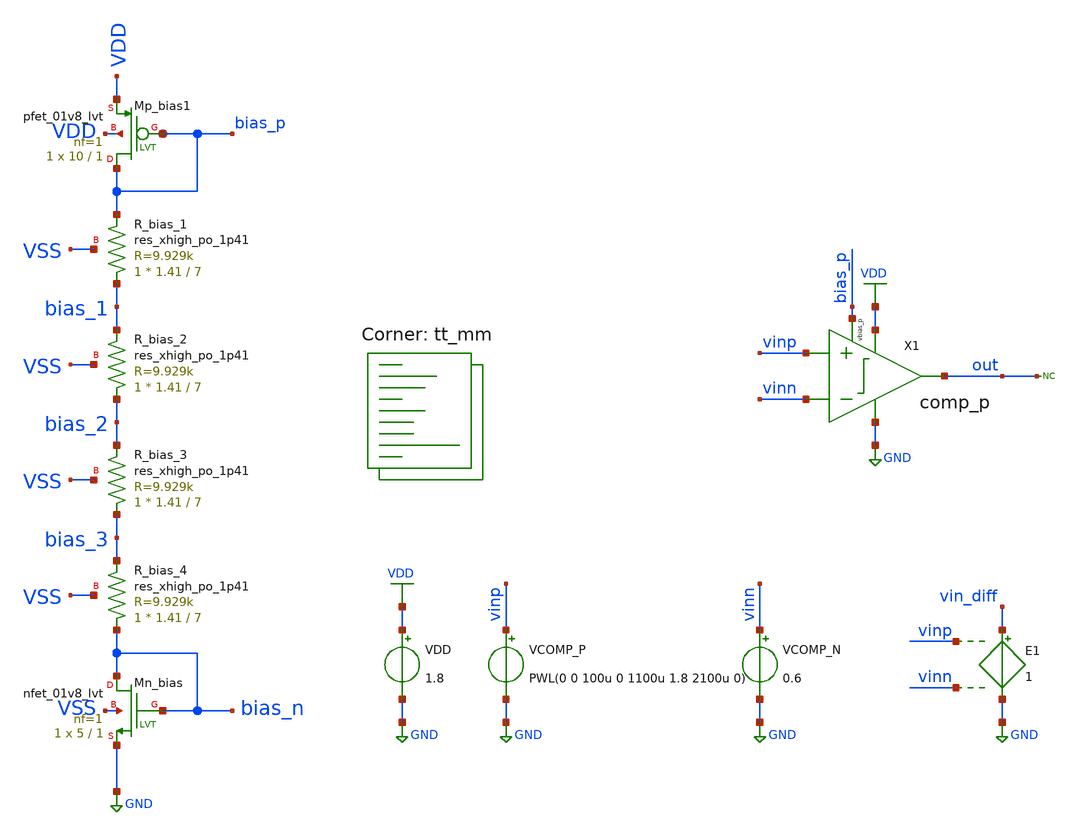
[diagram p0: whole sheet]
** sch_path: xsch/tb/comp_p/tb_comp_p_tran_sweep_mc.sch
**.subckt tb_comp_p_tran_sweep_mc
VDD VDD GND 1.8
* noconn out
VCOMP_N vinn GND 0.6
VCOMP_P vinp GND PWL(0 0 100u 0 1100u 1.8 2100u 0)
E1 vin_diff GND vinp vinn 1
XR_bias_1 bias_1 bias_p VSS sky130_fd_pr__res_xhigh_po_1p41 L=7 mult=1 m=1
XMn_bias bias_n bias_n GND VSS sky130_fd_pr__nfet_01v8_lvt L=1 W=5 nf=1 ad='int((nf+1)/2) * W/nf * 0.29'
+ as='int((nf+2)/2) * W/nf * 0.29' pd='2*int((nf+1)/2) * (W/nf + 0.29)' ps='2*int((nf+2)/2) * (W/nf + 0.29)'
+ nrd='0.29 / W' nrs='0.29 / W' sa=0 sb=0 sd=0 mult=1 m=1
XMp_bias1 bias_p bias_p VDD VDD sky130_fd_pr__pfet_01v8_lvt L=1 W=10 nf=1 ad='int((nf+1)/2) * W/nf * 0.29'
+ as='int((nf+2)/2) * W/nf * 0.29' pd='2*int((nf+1)/2) * (W/nf + 0.29)' ps='2*int((nf+2)/2) * (W/nf + 0.29)'
+ nrd='0.29 / W' nrs='0.29 / W' sa=0 sb=0 sd=0 mult=1 m=1
XR_bias_2 bias_2 bias_1 VSS sky130_fd_pr__res_xhigh_po_1p41 L=7 mult=1 m=1
XR_bias_3 bias_3 bias_2 VSS sky130_fd_pr__res_xhigh_po_1p41 L=7 mult=1 m=1
XR_bias_4 bias_n bias_3 VSS sky130_fd_pr__res_xhigh_po_1p41 L=7 mult=1 m=1
X1 vinp vinn bias_p out VDD GND comp_p
**** begin user architecture code



* control language script
.save X_COMP_P.latch_right
.save X_COMP_P.latch_left
.save vinp vinn out vdd
.save X_COMP_P.tail
.save bias_n

.control
set singlescale
set wr_vecnames
let mc_runs = 200
let run = 0

let v_th = vector(mc_runs)
let v_tl = vector(mc_runs)
let v_hyst = vector(mc_runs)
let v_offset = vector(mc_runs)
let design_point = vector(mc_runs) ; lets me plot quantities vs mc run

while run <= mc_runs
	tran 0.1u 2100u

	meas tran v_cross_lh FIND v(vinp) when v(out)=0.9 RISE=1
	meas tran v_cross_hl FIND v(vinp) when v(out)=0.9 FALL=1

	let v_th[run] = v_cross_lh-0.6
	let v_tl[run] = v_cross_hl-0.6
	let v_hyst[run] = v_th[run] - v_tl[run]
	let v_offset[run] = v_th[run] + v_tl[run]

	echo V_th: $&v_th
	echo V_tl: $&v_tl
	echo V_hyst: $&v_hyst
	echo V_offset: $&v_offset

	reset
	let run = run + 1;
end

plot tran1.v(out) tran2.v(out) tran3.v(out) tran4.v(out) tran5.v(out) tran6.v(out) tran7.v(out)
+ tran8.v(out) tran9.v(out) tran10.v(out) tran1.v(vinp) tran1.v(vinn)

wrdata tb_comp_p_tran_sweep_mc_vth.txt v_th vs design_point
wrdata tb_comp_p_tran_sweep_mc_vhyst.txt v_hyst vs design_point

rusage

.endc
.end



.lib $::SKYWATER_MODELS/sky130.lib.spice tt_mm
**** end user architecture code
**.ends

* expanding   symbol:  /home/bmott/ttsky25b_tiny_chaos/xsch/ip/comparators/comp_p/comp_p.sym # of
*+ pins=6
** sym_path: /home/bmott/ttsky25b_tiny_chaos/xsch/ip/comparators/comp_p/comp_p.sym
** sch_path: /home/bmott/ttsky25b_tiny_chaos/xsch/ip/comparators/comp_p/comp_p.sch
.subckt comp_p vinp vinn vbias_p vout vdd vss
*.iopin vdd
*.iopin vss
*.ipin vbias_p
*.ipin vinn
*.ipin vinp
*.opin vout
XMp_inn1 latch_left vinn tail vdd sky130_fd_pr__pfet_01v8_lvt L=0.35 W=10 nf=1 ad='int((nf+1)/2) * W/nf * 0.29'
+ as='int((nf+2)/2) * W/nf * 0.29' pd='2*int((nf+1)/2) * (W/nf + 0.29)' ps='2*int((nf+2)/2) * (W/nf + 0.29)'
+ nrd='0.29 / W' nrs='0.29 / W' sa=0 sb=0 sd=0 mult=4 m=4
XMp_inp1 latch_right vinp tail vdd sky130_fd_pr__pfet_01v8_lvt L=0.35 W=10 nf=1 ad='int((nf+1)/2) * W/nf * 0.29'
+ as='int((nf+2)/2) * W/nf * 0.29' pd='2*int((nf+1)/2) * (W/nf + 0.29)' ps='2*int((nf+2)/2) * (W/nf + 0.29)'
+ nrd='0.29 / W' nrs='0.29 / W' sa=0 sb=0 sd=0 mult=4 m=4
XMn_diode_left1 latch_left latch_left vss vss sky130_fd_pr__nfet_01v8_lvt L=1 W=4 nf=1 ad='int((nf+1)/2) * W/nf * 0.29'
+ as='int((nf+2)/2) * W/nf * 0.29' pd='2*int((nf+1)/2) * (W/nf + 0.29)' ps='2*int((nf+2)/2) * (W/nf + 0.29)'
+ nrd='0.29 / W' nrs='0.29 / W' sa=0 sb=0 sd=0 mult=1 m=1
XMn_cs_left latch_right latch_left vss vss sky130_fd_pr__nfet_01v8_lvt L=1 W=5 nf=1 ad='int((nf+1)/2) * W/nf * 0.29'
+ as='int((nf+2)/2) * W/nf * 0.29' pd='2*int((nf+1)/2) * (W/nf + 0.29)' ps='2*int((nf+2)/2) * (W/nf + 0.29)'
+ nrd='0.29 / W' nrs='0.29 / W' sa=0 sb=0 sd=0 mult=1 m=1
XMn_diode_right latch_right latch_right vss vss sky130_fd_pr__nfet_01v8_lvt L=1 W=4 nf=1 ad='int((nf+1)/2) * W/nf * 0.29'
+ as='int((nf+2)/2) * W/nf * 0.29' pd='2*int((nf+1)/2) * (W/nf + 0.29)' ps='2*int((nf+2)/2) * (W/nf + 0.29)'
+ nrd='0.29 / W' nrs='0.29 / W' sa=0 sb=0 sd=0 mult=1 m=1
XMn_cs_right1 latch_left latch_right vss vss sky130_fd_pr__nfet_01v8_lvt L=1 W=5 nf=1 ad='int((nf+1)/2) * W/nf * 0.29'
+ as='int((nf+2)/2) * W/nf * 0.29' pd='2*int((nf+1)/2) * (W/nf + 0.29)' ps='2*int((nf+2)/2) * (W/nf + 0.29)'
+ nrd='0.29 / W' nrs='0.29 / W' sa=0 sb=0 sd=0 mult=1 m=1
XMp_tail tail vbias_p vdd vdd sky130_fd_pr__pfet_01v8_lvt L=1 W=10 nf=1 ad='int((nf+1)/2) * W/nf * 0.29'
+ as='int((nf+2)/2) * W/nf * 0.29' pd='2*int((nf+1)/2) * (W/nf + 0.29)' ps='2*int((nf+2)/2) * (W/nf + 0.29)'
+ nrd='0.29 / W' nrs='0.29 / W' sa=0 sb=0 sd=0 mult=1 m=1
XMn_out_right vout latch_right vss vss sky130_fd_pr__nfet_01v8_lvt L=1 W=5 nf=1 ad='int((nf+1)/2) * W/nf * 0.29'
+ as='int((nf+2)/2) * W/nf * 0.29' pd='2*int((nf+1)/2) * (W/nf + 0.29)' ps='2*int((nf+2)/2) * (W/nf + 0.29)'
+ nrd='0.29 / W' nrs='0.29 / W' sa=0 sb=0 sd=0 mult=1 m=1
XMn_out_left out_left latch_left vss vss sky130_fd_pr__nfet_01v8_lvt L=1 W=5 nf=1 ad='int((nf+1)/2) * W/nf * 0.29'
+ as='int((nf+2)/2) * W/nf * 0.29' pd='2*int((nf+1)/2) * (W/nf + 0.29)' ps='2*int((nf+2)/2) * (W/nf + 0.29)'
+ nrd='0.29 / W' nrs='0.29 / W' sa=0 sb=0 sd=0 mult=1 m=1
XMp_diode_left1 out_left out_left vdd vdd sky130_fd_pr__pfet_01v8_lvt L=1 W=8 nf=1 ad='int((nf+1)/2) * W/nf * 0.29'
+ as='int((nf+2)/2) * W/nf * 0.29' pd='2*int((nf+1)/2) * (W/nf + 0.29)' ps='2*int((nf+2)/2) * (W/nf + 0.29)'
+ nrd='0.29 / W' nrs='0.29 / W' sa=0 sb=0 sd=0 mult=1 m=1
XMp_out vout out_left vdd vdd sky130_fd_pr__pfet_01v8_lvt L=1 W=8 nf=1 ad='int((nf+1)/2) * W/nf * 0.29'
+ as='int((nf+2)/2) * W/nf * 0.29' pd='2*int((nf+1)/2) * (W/nf + 0.29)' ps='2*int((nf+2)/2) * (W/nf + 0.29)'
+ nrd='0.29 / W' nrs='0.29 / W' sa=0 sb=0 sd=0 mult=1 m=1
.ends

.GLOBAL VDD
.GLOBAL GND
.end
